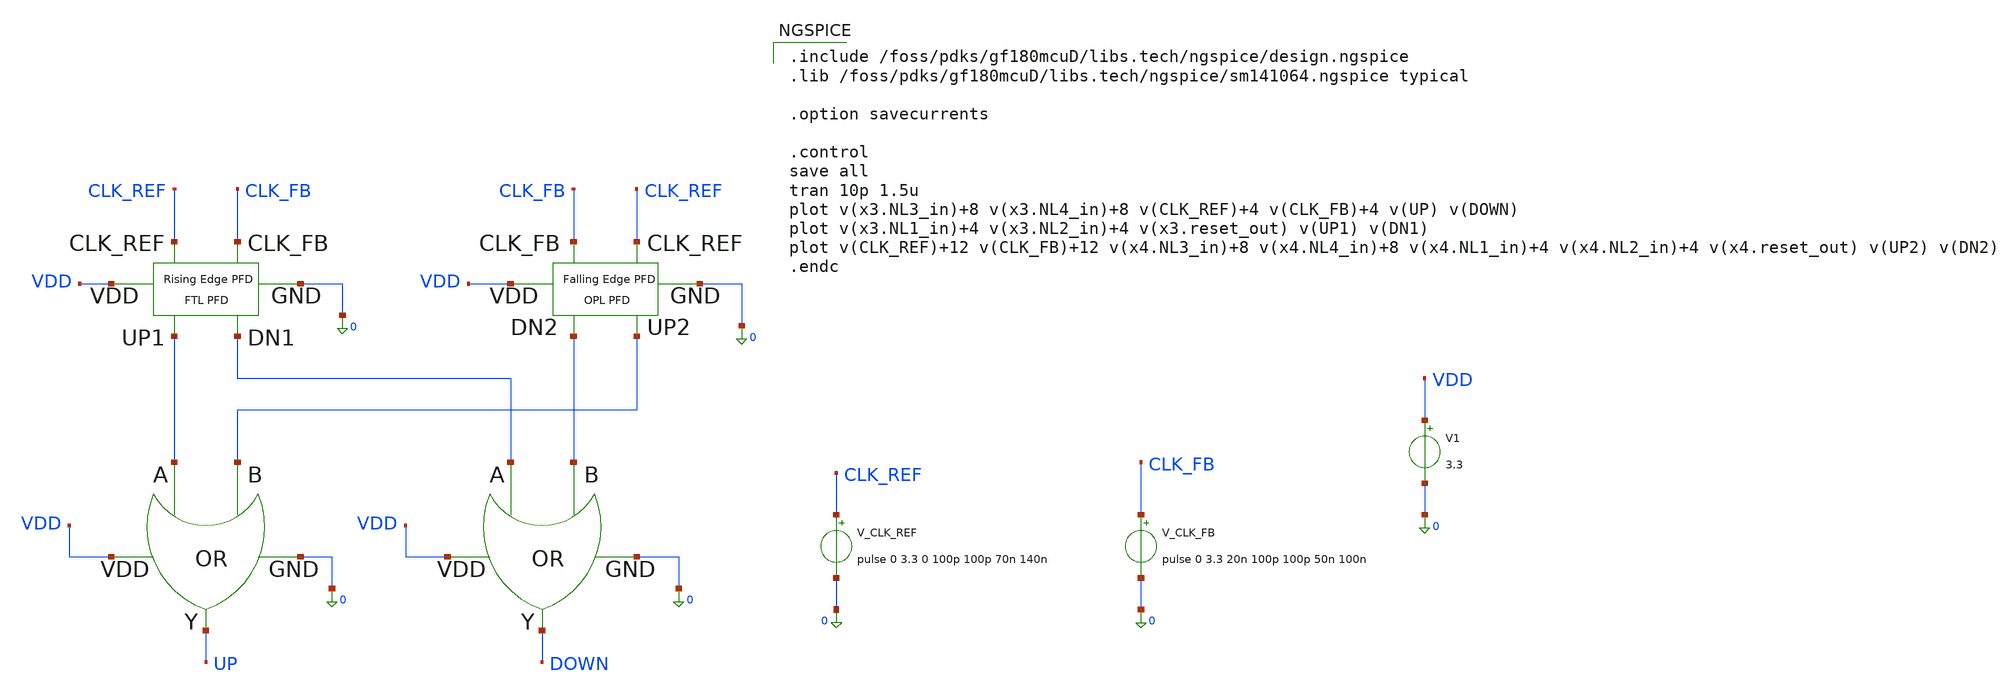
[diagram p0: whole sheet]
** sch_path: PFD/DELD_PFD.sch
**.subckt DELD_PFD
x1 0 DN1 DN2 VDD DOWN OR
x2 0 UP1 UP2 VDD UP OR
x3 DN1 UP1 CLK_FB CLK_REF VDD 0 FTL_PFD
x4 UP2 DN2 CLK_REF CLK_FB VDD 0 OPL_PFD
V1 VDD 0 3.3
.save i(v1)
V_CLK_REF CLK_REF 0 pulse 0 3.3 0 100p 100p 70n 140n
.save i(v_clk_ref)
V_CLK_FB CLK_FB 0 pulse 0 3.3 20n 100p 100p 50n 100n
.save i(v_clk_fb)
**** begin user architecture code

.include /foss/pdks/gf180mcuD/libs.tech/ngspice/design.ngspice
.lib /foss/pdks/gf180mcuD/libs.tech/ngspice/sm141064.ngspice typical

.option savecurrents

.control
save all
tran 10p 1.5u
plot v(x3.NL3_in)+8 v(x3.NL4_in)+8 v(CLK_REF)+4 v(CLK_FB)+4 v(UP) v(DOWN)
plot v(x3.NL1_in)+4 v(x3.NL2_in)+4 v(x3.reset_out) v(UP1) v(DN1)
plot v(CLK_REF)+12 v(CLK_FB)+12 v(x4.NL3_in)+8 v(x4.NL4_in)+8 v(x4.NL1_in)+4 v(x4.NL2_in)+4
+ v(x4.reset_out) v(UP2) v(DN2)
.endc

**** end user architecture code
**.ends

* expanding   symbol:  OR.sym # of pins=5
** sym_path: PFD/OR.sym
** sch_path: PFD/OR.sch
.subckt OR GND A B VDD Y
*.opin Y
*.ipin GND
*.ipin VDD
*.ipin A
*.ipin B
XM3 net2 A GND GND nfet_03v3 L=0.28u W=0.22u nf=1 ad='int((nf+1)/2) * W/nf * 0.18u' as='int((nf+2)/2) * W/nf * 0.18u'
+ pd='2*int((nf+1)/2) * (W/nf + 0.18u)' ps='2*int((nf+2)/2) * (W/nf + 0.18u)' nrd='0.18u / W' nrs='0.18u / W'
+ sa=0 sb=0 sd=0 m=1
XM2 net1 A net3 VDD pfet_03v3 L=0.28u W=0.22u nf=1 ad='int((nf+1)/2) * W/nf * 0.18u' as='int((nf+2)/2) * W/nf * 0.18u'
+ pd='2*int((nf+1)/2) * (W/nf + 0.18u)' ps='2*int((nf+2)/2) * (W/nf + 0.18u)' nrd='0.18u / W' nrs='0.18u / W'
+ sa=0 sb=0 sd=0 m=3
XM4 net2 B net1 net4 pfet_03v3 L=0.28u W=0.22u nf=1 ad='int((nf+1)/2) * W/nf * 0.18u' as='int((nf+2)/2) * W/nf * 0.18u'
+ pd='2*int((nf+1)/2) * (W/nf + 0.18u)' ps='2*int((nf+2)/2) * (W/nf + 0.18u)' nrd='0.18u / W' nrs='0.18u / W'
+ sa=0 sb=0 sd=0 m=3
XM1 net2 B GND GND nfet_03v3 L=0.28u W=0.22u nf=1 ad='int((nf+1)/2) * W/nf * 0.18u' as='int((nf+2)/2) * W/nf * 0.18u'
+ pd='2*int((nf+1)/2) * (W/nf + 0.18u)' ps='2*int((nf+2)/2) * (W/nf + 0.18u)' nrd='0.18u / W' nrs='0.18u / W'
+ sa=0 sb=0 sd=0 m=1
XM29 Y net2 VDD VDD pfet_03v3 L=0.28u W=0.22u nf=1 ad='int((nf+1)/2) * W/nf * 0.18u' as='int((nf+2)/2) * W/nf * 0.18u'
+ pd='2*int((nf+1)/2) * (W/nf + 0.18u)' ps='2*int((nf+2)/2) * (W/nf + 0.18u)' nrd='0.18u / W' nrs='0.18u / W'
+ sa=0 sb=0 sd=0 m=3
XM30 Y net2 GND GND nfet_03v3 L=0.28u W=0.22u nf=1 ad='int((nf+1)/2) * W/nf * 0.18u' as='int((nf+2)/2) * W/nf * 0.18u'
+ pd='2*int((nf+1)/2) * (W/nf + 0.18u)' ps='2*int((nf+2)/2) * (W/nf + 0.18u)' nrd='0.18u / W' nrs='0.18u / W'
+ sa=0 sb=0 sd=0 m=1
.ends


* expanding   symbol:  FTL_PFD.sym # of pins=6
** sym_path: PFD/FTL_PFD.sym
** sch_path: PFD/FTL_PFD.sch
.subckt FTL_PFD DN1 UP1 CLK_FB CLK_REF VDD GND
*.opin UP1
*.opin DN1
*.ipin CLK_FB
*.ipin CLK_REF
*.iopin VDD
*.iopin GND
XM1 net1 net3 VDD VDD pfet_03v3 L=0.28u W=0.22u nf=1 ad='int((nf+1)/2) * W/nf * 0.18u' as='int((nf+2)/2) * W/nf * 0.18u'
+ pd='2*int((nf+1)/2) * (W/nf + 0.18u)' ps='2*int((nf+2)/2) * (W/nf + 0.18u)' nrd='0.18u / W' nrs='0.18u / W'
+ sa=0 sb=0 sd=0 m=3
XM4 net2 net3 GND GND nfet_03v3 L=0.28u W=0.22u nf=1 ad='int((nf+1)/2) * W/nf * 0.18u' as='int((nf+2)/2) * W/nf * 0.18u'
+ pd='2*int((nf+1)/2) * (W/nf + 0.18u)' ps='2*int((nf+2)/2) * (W/nf + 0.18u)' nrd='0.18u / W' nrs='0.18u / W'
+ sa=0 sb=0 sd=0 m=1
XM2 net2 CLK_REF net1 VDD pfet_03v3 L=0.28u W=0.22u nf=1 ad='int((nf+1)/2) * W/nf * 0.18u' as='int((nf+2)/2) * W/nf * 0.18u'
+ pd='2*int((nf+1)/2) * (W/nf + 0.18u)' ps='2*int((nf+2)/2) * (W/nf + 0.18u)' nrd='0.18u / W' nrs='0.18u / W'
+ sa=0 sb=0 sd=0 m=3
XM3 net2 CLK_REF GND GND nfet_03v3 L=0.28u W=0.22u nf=1 ad='int((nf+1)/2) * W/nf * 0.18u' as='int((nf+2)/2) * W/nf * 0.18u'
+ pd='2*int((nf+1)/2) * (W/nf + 0.18u)' ps='2*int((nf+2)/2) * (W/nf + 0.18u)' nrd='0.18u / W' nrs='0.18u / W'
+ sa=0 sb=0 sd=0 m=1
XM5 net4 net2 VDD VDD pfet_03v3 L=0.28u W=0.22u nf=1 ad='int((nf+1)/2) * W/nf * 0.18u' as='int((nf+2)/2) * W/nf * 0.18u'
+ pd='2*int((nf+1)/2) * (W/nf + 0.18u)' ps='2*int((nf+2)/2) * (W/nf + 0.18u)' nrd='0.18u / W' nrs='0.18u / W'
+ sa=0 sb=0 sd=0 m=3
XM6 net5 CLK_REF net4 VDD pfet_03v3 L=0.28u W=0.22u nf=1 ad='int((nf+1)/2) * W/nf * 0.18u' as='int((nf+2)/2) * W/nf * 0.18u'
+ pd='2*int((nf+1)/2) * (W/nf + 0.18u)' ps='2*int((nf+2)/2) * (W/nf + 0.18u)' nrd='0.18u / W' nrs='0.18u / W'
+ sa=0 sb=0 sd=0 m=3
XM7 net5 net2 GND GND nfet_03v3 L=0.28u W=0.22u nf=1 ad='int((nf+1)/2) * W/nf * 0.18u' as='int((nf+2)/2) * W/nf * 0.18u'
+ pd='2*int((nf+1)/2) * (W/nf + 0.18u)' ps='2*int((nf+2)/2) * (W/nf + 0.18u)' nrd='0.18u / W' nrs='0.18u / W'
+ sa=0 sb=0 sd=0 m=1
XM9 net6 CLK_REF_bar VDD VDD pfet_03v3 L=0.28u W=0.22u nf=1 ad='int((nf+1)/2) * W/nf * 0.18u' as='int((nf+2)/2) * W/nf * 0.18u'
+ pd='2*int((nf+1)/2) * (W/nf + 0.18u)' ps='2*int((nf+2)/2) * (W/nf + 0.18u)' nrd='0.18u / W' nrs='0.18u / W'
+ sa=0 sb=0 sd=0 m=3
XM10 net7 net5 GND GND nfet_03v3 L=0.28u W=0.22u nf=1 ad='int((nf+1)/2) * W/nf * 0.18u' as='int((nf+2)/2) * W/nf * 0.18u'
+ pd='2*int((nf+1)/2) * (W/nf + 0.18u)' ps='2*int((nf+2)/2) * (W/nf + 0.18u)' nrd='0.18u / W' nrs='0.18u / W'
+ sa=0 sb=0 sd=0 m=1
XM8 net7 net5 net6 VDD pfet_03v3 L=0.28u W=0.22u nf=1 ad='int((nf+1)/2) * W/nf * 0.18u' as='int((nf+2)/2) * W/nf * 0.18u'
+ pd='2*int((nf+1)/2) * (W/nf + 0.18u)' ps='2*int((nf+2)/2) * (W/nf + 0.18u)' nrd='0.18u / W' nrs='0.18u / W'
+ sa=0 sb=0 sd=0 m=3
XM11 net7 CLK_REF_bar GND GND nfet_03v3 L=0.28u W=0.22u nf=1 ad='int((nf+1)/2) * W/nf * 0.18u' as='int((nf+2)/2) * W/nf * 0.18u'
+ pd='2*int((nf+1)/2) * (W/nf + 0.18u)' ps='2*int((nf+2)/2) * (W/nf + 0.18u)' nrd='0.18u / W' nrs='0.18u / W'
+ sa=0 sb=0 sd=0 m=1
XM12 net8 net7 VDD VDD pfet_03v3 L=0.28u W=0.22u nf=1 ad='int((nf+1)/2) * W/nf * 0.18u' as='int((nf+2)/2) * W/nf * 0.18u'
+ pd='2*int((nf+1)/2) * (W/nf + 0.18u)' ps='2*int((nf+2)/2) * (W/nf + 0.18u)' nrd='0.18u / W' nrs='0.18u / W'
+ sa=0 sb=0 sd=0 m=3
XM13 UP1 CLK_REF_bar net8 VDD pfet_03v3 L=0.28u W=0.22u nf=1 ad='int((nf+1)/2) * W/nf * 0.18u' as='int((nf+2)/2) * W/nf * 0.18u'
+ pd='2*int((nf+1)/2) * (W/nf + 0.18u)' ps='2*int((nf+2)/2) * (W/nf + 0.18u)' nrd='0.18u / W' nrs='0.18u / W'
+ sa=0 sb=0 sd=0 m=3
XM14 UP1 net7 GND GND nfet_03v3 L=0.28u W=0.22u nf=1 ad='int((nf+1)/2) * W/nf * 0.18u' as='int((nf+2)/2) * W/nf * 0.18u'
+ pd='2*int((nf+1)/2) * (W/nf + 0.18u)' ps='2*int((nf+2)/2) * (W/nf + 0.18u)' nrd='0.18u / W' nrs='0.18u / W'
+ sa=0 sb=0 sd=0 m=1
XM15 net9 net3 VDD VDD pfet_03v3 L=0.28u W=0.22u nf=1 ad='int((nf+1)/2) * W/nf * 0.18u' as='int((nf+2)/2) * W/nf * 0.18u'
+ pd='2*int((nf+1)/2) * (W/nf + 0.18u)' ps='2*int((nf+2)/2) * (W/nf + 0.18u)' nrd='0.18u / W' nrs='0.18u / W'
+ sa=0 sb=0 sd=0 m=3
XM16 net10 net3 GND GND nfet_03v3 L=0.28u W=0.22u nf=1 ad='int((nf+1)/2) * W/nf * 0.18u' as='int((nf+2)/2) * W/nf * 0.18u'
+ pd='2*int((nf+1)/2) * (W/nf + 0.18u)' ps='2*int((nf+2)/2) * (W/nf + 0.18u)' nrd='0.18u / W' nrs='0.18u / W'
+ sa=0 sb=0 sd=0 m=1
XM17 net10 CLK_FB net9 VDD pfet_03v3 L=0.28u W=0.22u nf=1 ad='int((nf+1)/2) * W/nf * 0.18u' as='int((nf+2)/2) * W/nf * 0.18u'
+ pd='2*int((nf+1)/2) * (W/nf + 0.18u)' ps='2*int((nf+2)/2) * (W/nf + 0.18u)' nrd='0.18u / W' nrs='0.18u / W'
+ sa=0 sb=0 sd=0 m=3
XM18 net10 CLK_FB GND GND nfet_03v3 L=0.28u W=0.22u nf=1 ad='int((nf+1)/2) * W/nf * 0.18u' as='int((nf+2)/2) * W/nf * 0.18u'
+ pd='2*int((nf+1)/2) * (W/nf + 0.18u)' ps='2*int((nf+2)/2) * (W/nf + 0.18u)' nrd='0.18u / W' nrs='0.18u / W'
+ sa=0 sb=0 sd=0 m=1
XM19 net11 net10 VDD VDD pfet_03v3 L=0.28u W=0.22u nf=1 ad='int((nf+1)/2) * W/nf * 0.18u' as='int((nf+2)/2) * W/nf * 0.18u'
+ pd='2*int((nf+1)/2) * (W/nf + 0.18u)' ps='2*int((nf+2)/2) * (W/nf + 0.18u)' nrd='0.18u / W' nrs='0.18u / W'
+ sa=0 sb=0 sd=0 m=3
XM20 net12 CLK_FB net11 VDD pfet_03v3 L=0.28u W=0.22u nf=1 ad='int((nf+1)/2) * W/nf * 0.18u' as='int((nf+2)/2) * W/nf * 0.18u'
+ pd='2*int((nf+1)/2) * (W/nf + 0.18u)' ps='2*int((nf+2)/2) * (W/nf + 0.18u)' nrd='0.18u / W' nrs='0.18u / W'
+ sa=0 sb=0 sd=0 m=3
XM21 net12 net10 GND GND nfet_03v3 L=0.28u W=0.22u nf=1 ad='int((nf+1)/2) * W/nf * 0.18u' as='int((nf+2)/2) * W/nf * 0.18u'
+ pd='2*int((nf+1)/2) * (W/nf + 0.18u)' ps='2*int((nf+2)/2) * (W/nf + 0.18u)' nrd='0.18u / W' nrs='0.18u / W'
+ sa=0 sb=0 sd=0 m=1
XM22 net13 CLK_FB_bar VDD VDD pfet_03v3 L=0.28u W=0.22u nf=1 ad='int((nf+1)/2) * W/nf * 0.18u' as='int((nf+2)/2) * W/nf * 0.18u'
+ pd='2*int((nf+1)/2) * (W/nf + 0.18u)' ps='2*int((nf+2)/2) * (W/nf + 0.18u)' nrd='0.18u / W' nrs='0.18u / W'
+ sa=0 sb=0 sd=0 m=3
XM23 net14 net12 GND GND nfet_03v3 L=0.28u W=0.22u nf=1 ad='int((nf+1)/2) * W/nf * 0.18u' as='int((nf+2)/2) * W/nf * 0.18u'
+ pd='2*int((nf+1)/2) * (W/nf + 0.18u)' ps='2*int((nf+2)/2) * (W/nf + 0.18u)' nrd='0.18u / W' nrs='0.18u / W'
+ sa=0 sb=0 sd=0 m=1
XM24 net14 net12 net13 VDD pfet_03v3 L=0.28u W=0.22u nf=1 ad='int((nf+1)/2) * W/nf * 0.18u' as='int((nf+2)/2) * W/nf * 0.18u'
+ pd='2*int((nf+1)/2) * (W/nf + 0.18u)' ps='2*int((nf+2)/2) * (W/nf + 0.18u)' nrd='0.18u / W' nrs='0.18u / W'
+ sa=0 sb=0 sd=0 m=3
XM25 net14 CLK_FB_bar GND GND nfet_03v3 L=0.28u W=0.22u nf=1 ad='int((nf+1)/2) * W/nf * 0.18u' as='int((nf+2)/2) * W/nf * 0.18u'
+ pd='2*int((nf+1)/2) * (W/nf + 0.18u)' ps='2*int((nf+2)/2) * (W/nf + 0.18u)' nrd='0.18u / W' nrs='0.18u / W'
+ sa=0 sb=0 sd=0 m=1
XM26 net15 net14 VDD VDD pfet_03v3 L=0.28u W=0.22u nf=1 ad='int((nf+1)/2) * W/nf * 0.18u' as='int((nf+2)/2) * W/nf * 0.18u'
+ pd='2*int((nf+1)/2) * (W/nf + 0.18u)' ps='2*int((nf+2)/2) * (W/nf + 0.18u)' nrd='0.18u / W' nrs='0.18u / W'
+ sa=0 sb=0 sd=0 m=3
XM27 DN1 CLK_FB_bar net15 VDD pfet_03v3 L=0.28u W=0.22u nf=1 ad='int((nf+1)/2) * W/nf * 0.18u' as='int((nf+2)/2) * W/nf * 0.18u'
+ pd='2*int((nf+1)/2) * (W/nf + 0.18u)' ps='2*int((nf+2)/2) * (W/nf + 0.18u)' nrd='0.18u / W' nrs='0.18u / W'
+ sa=0 sb=0 sd=0 m=3
XM28 DN1 net14 GND GND nfet_03v3 L=0.28u W=0.22u nf=1 ad='int((nf+1)/2) * W/nf * 0.18u' as='int((nf+2)/2) * W/nf * 0.18u'
+ pd='2*int((nf+1)/2) * (W/nf + 0.18u)' ps='2*int((nf+2)/2) * (W/nf + 0.18u)' nrd='0.18u / W' nrs='0.18u / W'
+ sa=0 sb=0 sd=0 m=1
x1 GND UP1 DN1 VDD net3 XNOR
XM29 CLK_FB_bar CLK_FB VDD VDD pfet_03v3 L=0.28u W=0.22u nf=1 ad='int((nf+1)/2) * W/nf * 0.18u' as='int((nf+2)/2) * W/nf * 0.18u'
+ pd='2*int((nf+1)/2) * (W/nf + 0.18u)' ps='2*int((nf+2)/2) * (W/nf + 0.18u)' nrd='0.18u / W' nrs='0.18u / W'
+ sa=0 sb=0 sd=0 m=3
XM30 CLK_FB_bar CLK_FB GND GND nfet_03v3 L=0.28u W=0.22u nf=1 ad='int((nf+1)/2) * W/nf * 0.18u' as='int((nf+2)/2) * W/nf * 0.18u'
+ pd='2*int((nf+1)/2) * (W/nf + 0.18u)' ps='2*int((nf+2)/2) * (W/nf + 0.18u)' nrd='0.18u / W' nrs='0.18u / W'
+ sa=0 sb=0 sd=0 m=1
XM31 CLK_REF_bar CLK_REF VDD VDD pfet_03v3 L=0.28u W=0.22u nf=1 ad='int((nf+1)/2) * W/nf * 0.18u' as='int((nf+2)/2) * W/nf * 0.18u'
+ pd='2*int((nf+1)/2) * (W/nf + 0.18u)' ps='2*int((nf+2)/2) * (W/nf + 0.18u)' nrd='0.18u / W' nrs='0.18u / W'
+ sa=0 sb=0 sd=0 m=3
XM32 CLK_REF_bar CLK_REF GND GND nfet_03v3 L=0.28u W=0.22u nf=1 ad='int((nf+1)/2) * W/nf * 0.18u' as='int((nf+2)/2) * W/nf * 0.18u'
+ pd='2*int((nf+1)/2) * (W/nf + 0.18u)' ps='2*int((nf+2)/2) * (W/nf + 0.18u)' nrd='0.18u / W' nrs='0.18u / W'
+ sa=0 sb=0 sd=0 m=1
.ends


* expanding   symbol:  OPL_PFD.sym # of pins=6
** sym_path: PFD/OPL_PFD.sym
** sch_path: PFD/OPL_PFD.sch
.subckt OPL_PFD UP2 DN2 CLK_REF CLK_FB VDD GND
*.opin UP2
*.ipin CLK_FB
*.ipin CLK_REF
*.opin DN2
*.iopin VDD
*.iopin GND
XM1 net1 net3 VDD VDD pfet_03v3 L=0.28u W=0.22u nf=1 ad='int((nf+1)/2) * W/nf * 0.18u' as='int((nf+2)/2) * W/nf * 0.18u'
+ pd='2*int((nf+1)/2) * (W/nf + 0.18u)' ps='2*int((nf+2)/2) * (W/nf + 0.18u)' nrd='0.18u / W' nrs='0.18u / W'
+ sa=0 sb=0 sd=0 m=3
XM4 net2 net3 GND GND nfet_03v3 L=0.28u W=0.22u nf=1 ad='int((nf+1)/2) * W/nf * 0.18u' as='int((nf+2)/2) * W/nf * 0.18u'
+ pd='2*int((nf+1)/2) * (W/nf + 0.18u)' ps='2*int((nf+2)/2) * (W/nf + 0.18u)' nrd='0.18u / W' nrs='0.18u / W'
+ sa=0 sb=0 sd=0 m=1
XM5 net4 net1 VDD VDD pfet_03v3 L=0.28u W=0.22u nf=1 ad='int((nf+1)/2) * W/nf * 0.18u' as='int((nf+2)/2) * W/nf * 0.18u'
+ pd='2*int((nf+1)/2) * (W/nf + 0.18u)' ps='2*int((nf+2)/2) * (W/nf + 0.18u)' nrd='0.18u / W' nrs='0.18u / W'
+ sa=0 sb=0 sd=0 m=3
XM7 net5 net1 GND GND nfet_03v3 L=0.28u W=0.22u nf=1 ad='int((nf+1)/2) * W/nf * 0.18u' as='int((nf+2)/2) * W/nf * 0.18u'
+ pd='2*int((nf+1)/2) * (W/nf + 0.18u)' ps='2*int((nf+2)/2) * (W/nf + 0.18u)' nrd='0.18u / W' nrs='0.18u / W'
+ sa=0 sb=0 sd=0 m=1
XM9 net6 CLK_REF_bar VDD VDD pfet_03v3 L=0.28u W=0.22u nf=1 ad='int((nf+1)/2) * W/nf * 0.18u' as='int((nf+2)/2) * W/nf * 0.18u'
+ pd='2*int((nf+1)/2) * (W/nf + 0.18u)' ps='2*int((nf+2)/2) * (W/nf + 0.18u)' nrd='0.18u / W' nrs='0.18u / W'
+ sa=0 sb=0 sd=0 m=3
XM11 net13 CLK_REF_bar GND GND nfet_03v3 L=0.28u W=0.22u nf=1 ad='int((nf+1)/2) * W/nf * 0.18u' as='int((nf+2)/2) * W/nf * 0.18u'
+ pd='2*int((nf+1)/2) * (W/nf + 0.18u)' ps='2*int((nf+2)/2) * (W/nf + 0.18u)' nrd='0.18u / W' nrs='0.18u / W'
+ sa=0 sb=0 sd=0 m=1
XM12 net11 net6 VDD VDD pfet_03v3 L=0.28u W=0.22u nf=1 ad='int((nf+1)/2) * W/nf * 0.18u' as='int((nf+2)/2) * W/nf * 0.18u'
+ pd='2*int((nf+1)/2) * (W/nf + 0.18u)' ps='2*int((nf+2)/2) * (W/nf + 0.18u)' nrd='0.18u / W' nrs='0.18u / W'
+ sa=0 sb=0 sd=0 m=3
XM14 net12 net6 GND GND nfet_03v3 L=0.28u W=0.22u nf=1 ad='int((nf+1)/2) * W/nf * 0.18u' as='int((nf+2)/2) * W/nf * 0.18u'
+ pd='2*int((nf+1)/2) * (W/nf + 0.18u)' ps='2*int((nf+2)/2) * (W/nf + 0.18u)' nrd='0.18u / W' nrs='0.18u / W'
+ sa=0 sb=0 sd=0 m=1
XM2 net1 CLK_REF VDD VDD pfet_03v3 L=0.28u W=0.22u nf=1 ad='int((nf+1)/2) * W/nf * 0.18u' as='int((nf+2)/2) * W/nf * 0.18u'
+ pd='2*int((nf+1)/2) * (W/nf + 0.18u)' ps='2*int((nf+2)/2) * (W/nf + 0.18u)' nrd='0.18u / W' nrs='0.18u / W'
+ sa=0 sb=0 sd=0 m=3
XM6 net4 CLK_REF net5 GND nfet_03v3 L=0.28u W=0.22u nf=1 ad='int((nf+1)/2) * W/nf * 0.18u' as='int((nf+2)/2) * W/nf * 0.18u'
+ pd='2*int((nf+1)/2) * (W/nf + 0.18u)' ps='2*int((nf+2)/2) * (W/nf + 0.18u)' nrd='0.18u / W' nrs='0.18u / W'
+ sa=0 sb=0 sd=0 m=1
XM10 net6 net4 net13 GND nfet_03v3 L=0.28u W=0.22u nf=1 ad='int((nf+1)/2) * W/nf * 0.18u' as='int((nf+2)/2) * W/nf * 0.18u'
+ pd='2*int((nf+1)/2) * (W/nf + 0.18u)' ps='2*int((nf+2)/2) * (W/nf + 0.18u)' nrd='0.18u / W' nrs='0.18u / W'
+ sa=0 sb=0 sd=0 m=1
XM8 net6 net4 VDD VDD pfet_03v3 L=0.28u W=0.22u nf=1 ad='int((nf+1)/2) * W/nf * 0.18u' as='int((nf+2)/2) * W/nf * 0.18u'
+ pd='2*int((nf+1)/2) * (W/nf + 0.18u)' ps='2*int((nf+2)/2) * (W/nf + 0.18u)' nrd='0.18u / W' nrs='0.18u / W'
+ sa=0 sb=0 sd=0 m=3
XM13 net11 CLK_REF_bar net12 GND nfet_03v3 L=0.28u W=0.22u nf=1 ad='int((nf+1)/2) * W/nf * 0.18u' as='int((nf+2)/2) * W/nf * 0.18u'
+ pd='2*int((nf+1)/2) * (W/nf + 0.18u)' ps='2*int((nf+2)/2) * (W/nf + 0.18u)' nrd='0.18u / W' nrs='0.18u / W'
+ sa=0 sb=0 sd=0 m=1
XM15 UP2 net12 VDD VDD pfet_03v3 L=0.28u W=0.22u nf=1 ad='int((nf+1)/2) * W/nf * 0.18u' as='int((nf+2)/2) * W/nf * 0.18u'
+ pd='2*int((nf+1)/2) * (W/nf + 0.18u)' ps='2*int((nf+2)/2) * (W/nf + 0.18u)' nrd='0.18u / W' nrs='0.18u / W'
+ sa=0 sb=0 sd=0 m=3
XM16 UP2 net12 GND GND nfet_03v3 L=0.28u W=0.22u nf=1 ad='int((nf+1)/2) * W/nf * 0.18u' as='int((nf+2)/2) * W/nf * 0.18u'
+ pd='2*int((nf+1)/2) * (W/nf + 0.18u)' ps='2*int((nf+2)/2) * (W/nf + 0.18u)' nrd='0.18u / W' nrs='0.18u / W'
+ sa=0 sb=0 sd=0 m=1
XM17 CLK_FB_bar CLK_FB VDD VDD pfet_03v3 L=0.28u W=0.22u nf=1 ad='int((nf+1)/2) * W/nf * 0.18u' as='int((nf+2)/2) * W/nf * 0.18u'
+ pd='2*int((nf+1)/2) * (W/nf + 0.18u)' ps='2*int((nf+2)/2) * (W/nf + 0.18u)' nrd='0.18u / W' nrs='0.18u / W'
+ sa=0 sb=0 sd=0 m=3
XM18 CLK_FB_bar CLK_FB GND GND nfet_03v3 L=0.28u W=0.22u nf=1 ad='int((nf+1)/2) * W/nf * 0.18u' as='int((nf+2)/2) * W/nf * 0.18u'
+ pd='2*int((nf+1)/2) * (W/nf + 0.18u)' ps='2*int((nf+2)/2) * (W/nf + 0.18u)' nrd='0.18u / W' nrs='0.18u / W'
+ sa=0 sb=0 sd=0 m=1
XM19 CLK_REF_bar CLK_REF VDD VDD pfet_03v3 L=0.28u W=0.22u nf=1 ad='int((nf+1)/2) * W/nf * 0.18u' as='int((nf+2)/2) * W/nf * 0.18u'
+ pd='2*int((nf+1)/2) * (W/nf + 0.18u)' ps='2*int((nf+2)/2) * (W/nf + 0.18u)' nrd='0.18u / W' nrs='0.18u / W'
+ sa=0 sb=0 sd=0 m=3
XM20 CLK_REF_bar CLK_REF GND GND nfet_03v3 L=0.28u W=0.22u nf=1 ad='int((nf+1)/2) * W/nf * 0.18u' as='int((nf+2)/2) * W/nf * 0.18u'
+ pd='2*int((nf+1)/2) * (W/nf + 0.18u)' ps='2*int((nf+2)/2) * (W/nf + 0.18u)' nrd='0.18u / W' nrs='0.18u / W'
+ sa=0 sb=0 sd=0 m=1
XM3 net1 CLK_REF net2 GND nfet_03v3 L=0.28u W=0.22u nf=1 ad='int((nf+1)/2) * W/nf * 0.18u' as='int((nf+2)/2) * W/nf * 0.18u'
+ pd='2*int((nf+1)/2) * (W/nf + 0.18u)' ps='2*int((nf+2)/2) * (W/nf + 0.18u)' nrd='0.18u / W' nrs='0.18u / W'
+ sa=0 sb=0 sd=0 m=1
XM21 net14 net3 VDD VDD pfet_03v3 L=0.28u W=0.22u nf=1 ad='int((nf+1)/2) * W/nf * 0.18u' as='int((nf+2)/2) * W/nf * 0.18u'
+ pd='2*int((nf+1)/2) * (W/nf + 0.18u)' ps='2*int((nf+2)/2) * (W/nf + 0.18u)' nrd='0.18u / W' nrs='0.18u / W'
+ sa=0 sb=0 sd=0 m=3
XM22 net15 net3 GND GND nfet_03v3 L=0.28u W=0.22u nf=1 ad='int((nf+1)/2) * W/nf * 0.18u' as='int((nf+2)/2) * W/nf * 0.18u'
+ pd='2*int((nf+1)/2) * (W/nf + 0.18u)' ps='2*int((nf+2)/2) * (W/nf + 0.18u)' nrd='0.18u / W' nrs='0.18u / W'
+ sa=0 sb=0 sd=0 m=1
XM23 net9 net14 VDD VDD pfet_03v3 L=0.28u W=0.22u nf=1 ad='int((nf+1)/2) * W/nf * 0.18u' as='int((nf+2)/2) * W/nf * 0.18u'
+ pd='2*int((nf+1)/2) * (W/nf + 0.18u)' ps='2*int((nf+2)/2) * (W/nf + 0.18u)' nrd='0.18u / W' nrs='0.18u / W'
+ sa=0 sb=0 sd=0 m=3
XM24 net16 net14 GND GND nfet_03v3 L=0.28u W=0.22u nf=1 ad='int((nf+1)/2) * W/nf * 0.18u' as='int((nf+2)/2) * W/nf * 0.18u'
+ pd='2*int((nf+1)/2) * (W/nf + 0.18u)' ps='2*int((nf+2)/2) * (W/nf + 0.18u)' nrd='0.18u / W' nrs='0.18u / W'
+ sa=0 sb=0 sd=0 m=1
XM25 net10 CLK_FB_bar VDD VDD pfet_03v3 L=0.28u W=0.22u nf=1 ad='int((nf+1)/2) * W/nf * 0.18u' as='int((nf+2)/2) * W/nf * 0.18u'
+ pd='2*int((nf+1)/2) * (W/nf + 0.18u)' ps='2*int((nf+2)/2) * (W/nf + 0.18u)' nrd='0.18u / W' nrs='0.18u / W'
+ sa=0 sb=0 sd=0 m=3
XM26 net7 CLK_FB_bar GND GND nfet_03v3 L=0.28u W=0.22u nf=1 ad='int((nf+1)/2) * W/nf * 0.18u' as='int((nf+2)/2) * W/nf * 0.18u'
+ pd='2*int((nf+1)/2) * (W/nf + 0.18u)' ps='2*int((nf+2)/2) * (W/nf + 0.18u)' nrd='0.18u / W' nrs='0.18u / W'
+ sa=0 sb=0 sd=0 m=1
XM27 net17 net10 VDD VDD pfet_03v3 L=0.28u W=0.22u nf=1 ad='int((nf+1)/2) * W/nf * 0.18u' as='int((nf+2)/2) * W/nf * 0.18u'
+ pd='2*int((nf+1)/2) * (W/nf + 0.18u)' ps='2*int((nf+2)/2) * (W/nf + 0.18u)' nrd='0.18u / W' nrs='0.18u / W'
+ sa=0 sb=0 sd=0 m=3
XM28 net8 net10 GND GND nfet_03v3 L=0.28u W=0.22u nf=1 ad='int((nf+1)/2) * W/nf * 0.18u' as='int((nf+2)/2) * W/nf * 0.18u'
+ pd='2*int((nf+1)/2) * (W/nf + 0.18u)' ps='2*int((nf+2)/2) * (W/nf + 0.18u)' nrd='0.18u / W' nrs='0.18u / W'
+ sa=0 sb=0 sd=0 m=1
XM29 net14 CLK_FB VDD VDD pfet_03v3 L=0.28u W=0.22u nf=1 ad='int((nf+1)/2) * W/nf * 0.18u' as='int((nf+2)/2) * W/nf * 0.18u'
+ pd='2*int((nf+1)/2) * (W/nf + 0.18u)' ps='2*int((nf+2)/2) * (W/nf + 0.18u)' nrd='0.18u / W' nrs='0.18u / W'
+ sa=0 sb=0 sd=0 m=3
XM30 net9 CLK_FB net16 GND nfet_03v3 L=0.28u W=0.22u nf=1 ad='int((nf+1)/2) * W/nf * 0.18u' as='int((nf+2)/2) * W/nf * 0.18u'
+ pd='2*int((nf+1)/2) * (W/nf + 0.18u)' ps='2*int((nf+2)/2) * (W/nf + 0.18u)' nrd='0.18u / W' nrs='0.18u / W'
+ sa=0 sb=0 sd=0 m=1
XM31 net10 net9 net7 GND nfet_03v3 L=0.28u W=0.22u nf=1 ad='int((nf+1)/2) * W/nf * 0.18u' as='int((nf+2)/2) * W/nf * 0.18u'
+ pd='2*int((nf+1)/2) * (W/nf + 0.18u)' ps='2*int((nf+2)/2) * (W/nf + 0.18u)' nrd='0.18u / W' nrs='0.18u / W'
+ sa=0 sb=0 sd=0 m=1
XM32 net10 net9 VDD VDD pfet_03v3 L=0.28u W=0.22u nf=1 ad='int((nf+1)/2) * W/nf * 0.18u' as='int((nf+2)/2) * W/nf * 0.18u'
+ pd='2*int((nf+1)/2) * (W/nf + 0.18u)' ps='2*int((nf+2)/2) * (W/nf + 0.18u)' nrd='0.18u / W' nrs='0.18u / W'
+ sa=0 sb=0 sd=0 m=3
XM33 net17 CLK_FB_bar net8 GND nfet_03v3 L=0.28u W=0.22u nf=1 ad='int((nf+1)/2) * W/nf * 0.18u' as='int((nf+2)/2) * W/nf * 0.18u'
+ pd='2*int((nf+1)/2) * (W/nf + 0.18u)' ps='2*int((nf+2)/2) * (W/nf + 0.18u)' nrd='0.18u / W' nrs='0.18u / W'
+ sa=0 sb=0 sd=0 m=1
XM34 DN2 net8 VDD VDD pfet_03v3 L=0.28u W=0.22u nf=1 ad='int((nf+1)/2) * W/nf * 0.18u' as='int((nf+2)/2) * W/nf * 0.18u'
+ pd='2*int((nf+1)/2) * (W/nf + 0.18u)' ps='2*int((nf+2)/2) * (W/nf + 0.18u)' nrd='0.18u / W' nrs='0.18u / W'
+ sa=0 sb=0 sd=0 m=3
XM35 DN2 net8 GND GND nfet_03v3 L=0.28u W=0.22u nf=1 ad='int((nf+1)/2) * W/nf * 0.18u' as='int((nf+2)/2) * W/nf * 0.18u'
+ pd='2*int((nf+1)/2) * (W/nf + 0.18u)' ps='2*int((nf+2)/2) * (W/nf + 0.18u)' nrd='0.18u / W' nrs='0.18u / W'
+ sa=0 sb=0 sd=0 m=1
XM36 net14 CLK_FB net15 GND nfet_03v3 L=0.28u W=0.22u nf=1 ad='int((nf+1)/2) * W/nf * 0.18u' as='int((nf+2)/2) * W/nf * 0.18u'
+ pd='2*int((nf+1)/2) * (W/nf + 0.18u)' ps='2*int((nf+2)/2) * (W/nf + 0.18u)' nrd='0.18u / W' nrs='0.18u / W'
+ sa=0 sb=0 sd=0 m=1
x1 GND UP2 DN2 VDD net3 NAND
.ends


* expanding   symbol:  XNOR.sym # of pins=5
** sym_path: PFD/XNOR.sym
** sch_path: PFD/XNOR.sch
.subckt XNOR GND A B VDD Y
*.opin Y
*.ipin A
*.ipin B
*.iopin VDD
*.iopin GND
XM1 net1 A VDD VDD pfet_03v3 L=0.28u W=0.22u nf=1 ad='int((nf+1)/2) * W/nf * 0.18u' as='int((nf+2)/2) * W/nf * 0.18u'
+ pd='2*int((nf+1)/2) * (W/nf + 0.18u)' ps='2*int((nf+2)/2) * (W/nf + 0.18u)' nrd='0.18u / W' nrs='0.18u / W'
+ sa=0 sb=0 sd=0 m=1
XM2 Y A_bar net1 VDD pfet_03v3 L=0.28u W=0.22u nf=1 ad='int((nf+1)/2) * W/nf * 0.18u' as='int((nf+2)/2) * W/nf * 0.18u'
+ pd='2*int((nf+1)/2) * (W/nf + 0.18u)' ps='2*int((nf+2)/2) * (W/nf + 0.18u)' nrd='0.18u / W' nrs='0.18u / W'
+ sa=0 sb=0 sd=0 m=1
XM3 Y B_bar net2 GND nfet_03v3 L=0.28u W=0.22u nf=1 ad='int((nf+1)/2) * W/nf * 0.18u' as='int((nf+2)/2) * W/nf * 0.18u'
+ pd='2*int((nf+1)/2) * (W/nf + 0.18u)' ps='2*int((nf+2)/2) * (W/nf + 0.18u)' nrd='0.18u / W' nrs='0.18u / W'
+ sa=0 sb=0 sd=0 m=1
XM4 net2 A GND GND nfet_03v3 L=0.28u W=0.22u nf=1 ad='int((nf+1)/2) * W/nf * 0.18u' as='int((nf+2)/2) * W/nf * 0.18u'
+ pd='2*int((nf+1)/2) * (W/nf + 0.18u)' ps='2*int((nf+2)/2) * (W/nf + 0.18u)' nrd='0.18u / W' nrs='0.18u / W'
+ sa=0 sb=0 sd=0 m=1
XM5 net3 B_bar VDD VDD pfet_03v3 L=0.28u W=0.22u nf=1 ad='int((nf+1)/2) * W/nf * 0.18u' as='int((nf+2)/2) * W/nf * 0.18u'
+ pd='2*int((nf+1)/2) * (W/nf + 0.18u)' ps='2*int((nf+2)/2) * (W/nf + 0.18u)' nrd='0.18u / W' nrs='0.18u / W'
+ sa=0 sb=0 sd=0 m=1
XM6 Y B net3 VDD pfet_03v3 L=0.28u W=0.22u nf=1 ad='int((nf+1)/2) * W/nf * 0.18u' as='int((nf+2)/2) * W/nf * 0.18u'
+ pd='2*int((nf+1)/2) * (W/nf + 0.18u)' ps='2*int((nf+2)/2) * (W/nf + 0.18u)' nrd='0.18u / W' nrs='0.18u / W'
+ sa=0 sb=0 sd=0 m=1
XM7 Y A_bar net4 GND nfet_03v3 L=0.28u W=0.22u nf=1 ad='int((nf+1)/2) * W/nf * 0.18u' as='int((nf+2)/2) * W/nf * 0.18u'
+ pd='2*int((nf+1)/2) * (W/nf + 0.18u)' ps='2*int((nf+2)/2) * (W/nf + 0.18u)' nrd='0.18u / W' nrs='0.18u / W'
+ sa=0 sb=0 sd=0 m=1
XM8 net4 B GND GND nfet_03v3 L=0.28u W=0.22u nf=1 ad='int((nf+1)/2) * W/nf * 0.18u' as='int((nf+2)/2) * W/nf * 0.18u'
+ pd='2*int((nf+1)/2) * (W/nf + 0.18u)' ps='2*int((nf+2)/2) * (W/nf + 0.18u)' nrd='0.18u / W' nrs='0.18u / W'
+ sa=0 sb=0 sd=0 m=1
XM9 A_bar A VDD VDD pfet_03v3 L=0.28u W=0.22u nf=1 ad='int((nf+1)/2) * W/nf * 0.18u' as='int((nf+2)/2) * W/nf * 0.18u'
+ pd='2*int((nf+1)/2) * (W/nf + 0.18u)' ps='2*int((nf+2)/2) * (W/nf + 0.18u)' nrd='0.18u / W' nrs='0.18u / W'
+ sa=0 sb=0 sd=0 m=3
XM10 A_bar A GND GND nfet_03v3 L=0.28u W=0.22u nf=1 ad='int((nf+1)/2) * W/nf * 0.18u' as='int((nf+2)/2) * W/nf * 0.18u'
+ pd='2*int((nf+1)/2) * (W/nf + 0.18u)' ps='2*int((nf+2)/2) * (W/nf + 0.18u)' nrd='0.18u / W' nrs='0.18u / W'
+ sa=0 sb=0 sd=0 m=1
XM11 B_bar B VDD VDD pfet_03v3 L=0.28u W=0.22u nf=1 ad='int((nf+1)/2) * W/nf * 0.18u' as='int((nf+2)/2) * W/nf * 0.18u'
+ pd='2*int((nf+1)/2) * (W/nf + 0.18u)' ps='2*int((nf+2)/2) * (W/nf + 0.18u)' nrd='0.18u / W' nrs='0.18u / W'
+ sa=0 sb=0 sd=0 m=3
XM12 B_bar B GND GND nfet_03v3 L=0.28u W=0.22u nf=1 ad='int((nf+1)/2) * W/nf * 0.18u' as='int((nf+2)/2) * W/nf * 0.18u'
+ pd='2*int((nf+1)/2) * (W/nf + 0.18u)' ps='2*int((nf+2)/2) * (W/nf + 0.18u)' nrd='0.18u / W' nrs='0.18u / W'
+ sa=0 sb=0 sd=0 m=1
.ends


* expanding   symbol:  NAND.sym # of pins=5
** sym_path: PFD/NAND.sym
** sch_path: PFD/NAND.sch
.subckt NAND GND A B VDD Y
*.opin Y
*.ipin GND
*.ipin VDD
*.ipin A
*.ipin B
XM1 Y A VDD VDD pfet_03v3 L=0.28u W=0.22u nf=1 ad='int((nf+1)/2) * W/nf * 0.18u' as='int((nf+2)/2) * W/nf * 0.18u'
+ pd='2*int((nf+1)/2) * (W/nf + 0.18u)' ps='2*int((nf+2)/2) * (W/nf + 0.18u)' nrd='0.18u / W' nrs='0.18u / W'
+ sa=0 sb=0 sd=0 m=3
XM3 Y A net1 GND nfet_03v3 L=0.28u W=0.22u nf=1 ad='int((nf+1)/2) * W/nf * 0.18u' as='int((nf+2)/2) * W/nf * 0.18u'
+ pd='2*int((nf+1)/2) * (W/nf + 0.18u)' ps='2*int((nf+2)/2) * (W/nf + 0.18u)' nrd='0.18u / W' nrs='0.18u / W'
+ sa=0 sb=0 sd=0 m=1
XM4 net1 B GND GND nfet_03v3 L=0.28u W=0.22u nf=1 ad='int((nf+1)/2) * W/nf * 0.18u' as='int((nf+2)/2) * W/nf * 0.18u'
+ pd='2*int((nf+1)/2) * (W/nf + 0.18u)' ps='2*int((nf+2)/2) * (W/nf + 0.18u)' nrd='0.18u / W' nrs='0.18u / W'
+ sa=0 sb=0 sd=0 m=1
XM2 Y B VDD VDD pfet_03v3 L=0.28u W=0.22u nf=1 ad='int((nf+1)/2) * W/nf * 0.18u' as='int((nf+2)/2) * W/nf * 0.18u'
+ pd='2*int((nf+1)/2) * (W/nf + 0.18u)' ps='2*int((nf+2)/2) * (W/nf + 0.18u)' nrd='0.18u / W' nrs='0.18u / W'
+ sa=0 sb=0 sd=0 m=3
.ends

.end
